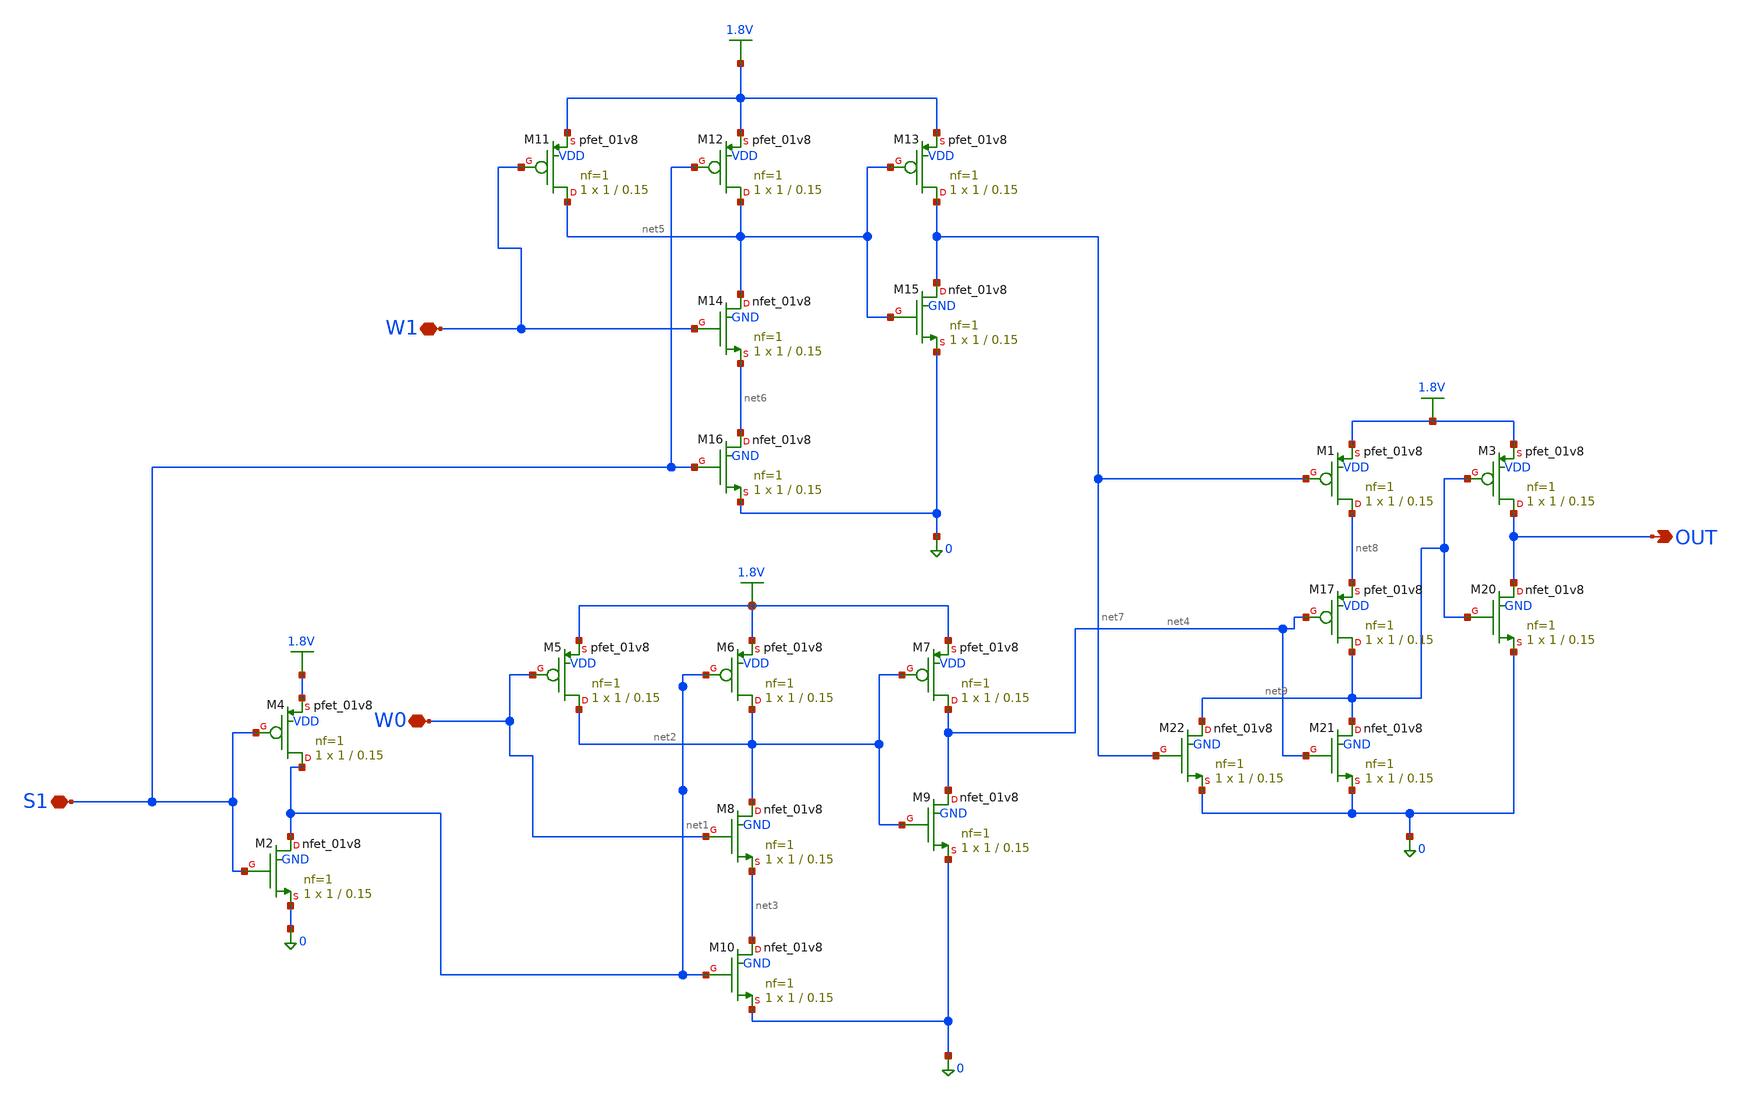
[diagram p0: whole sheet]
** sch_path: XUM21.sch
**.subckt XUM21 OUT W1 W0 S1
*.opin OUT
*.iopin W1
*.iopin W0
*.iopin S1
XM2 net1 S1 0 GND sky130_fd_pr__nfet_01v8 L=0.15 W=1 nf=1 ad='int((1 + 1)/2) * 1 / 1 * 0.29' as='int((1 + 2)/2) * 1 / 1 * 0.29'
+ pd='2*int((1 + 1)/2) * (1 / 1 + 0.29)' ps='2*int((1 + 2)/2) * (1 / 1 + 0.29)' nrd='0.29 / 1 ' nrs='0.29 / 1 '
+ sa=0 sb=0 sd=0 mult=1 m=1
XM8 net2 W0 net3 GND sky130_fd_pr__nfet_01v8 L=0.15 W=1 nf=1 ad='int((1 + 1)/2) * 1 / 1 * 0.29' as='int((1 + 2)/2) * 1 / 1 * 0.29'
+ pd='2*int((1 + 1)/2) * (1 / 1 + 0.29)' ps='2*int((1 + 2)/2) * (1 / 1 + 0.29)' nrd='0.29 / 1 ' nrs='0.29 / 1 '
+ sa=0 sb=0 sd=0 mult=1 m=1
XM9 net4 net2 0 GND sky130_fd_pr__nfet_01v8 L=0.15 W=1 nf=1 ad='int((1 + 1)/2) * 1 / 1 * 0.29' as='int((1 + 2)/2) * 1 / 1 * 0.29'
+ pd='2*int((1 + 1)/2) * (1 / 1 + 0.29)' ps='2*int((1 + 2)/2) * (1 / 1 + 0.29)' nrd='0.29 / 1 ' nrs='0.29 / 1 '
+ sa=0 sb=0 sd=0 mult=1 m=1
XM10 net3 net1 0 GND sky130_fd_pr__nfet_01v8 L=0.15 W=1 nf=1 ad='int((1 + 1)/2) * 1 / 1 * 0.29' as='int((1 + 2)/2) * 1 / 1 * 0.29'
+ pd='2*int((1 + 1)/2) * (1 / 1 + 0.29)' ps='2*int((1 + 2)/2) * (1 / 1 + 0.29)' nrd='0.29 / 1 ' nrs='0.29 / 1 '
+ sa=0 sb=0 sd=0 mult=1 m=1
XM14 net5 W1 net6 GND sky130_fd_pr__nfet_01v8 L=0.15 W=1 nf=1 ad='int((1 + 1)/2) * 1 / 1 * 0.29' as='int((1 + 2)/2) * 1 / 1 * 0.29'
+ pd='2*int((1 + 1)/2) * (1 / 1 + 0.29)' ps='2*int((1 + 2)/2) * (1 / 1 + 0.29)' nrd='0.29 / 1 ' nrs='0.29 / 1 '
+ sa=0 sb=0 sd=0 mult=1 m=1
XM15 net7 net5 0 GND sky130_fd_pr__nfet_01v8 L=0.15 W=1 nf=1 ad='int((1 + 1)/2) * 1 / 1 * 0.29' as='int((1 + 2)/2) * 1 / 1 * 0.29'
+ pd='2*int((1 + 1)/2) * (1 / 1 + 0.29)' ps='2*int((1 + 2)/2) * (1 / 1 + 0.29)' nrd='0.29 / 1 ' nrs='0.29 / 1 '
+ sa=0 sb=0 sd=0 mult=1 m=1
XM16 net6 S1 0 GND sky130_fd_pr__nfet_01v8 L=0.15 W=1 nf=1 ad='int((1 + 1)/2) * 1 / 1 * 0.29' as='int((1 + 2)/2) * 1 / 1 * 0.29'
+ pd='2*int((1 + 1)/2) * (1 / 1 + 0.29)' ps='2*int((1 + 2)/2) * (1 / 1 + 0.29)' nrd='0.29 / 1 ' nrs='0.29 / 1 '
+ sa=0 sb=0 sd=0 mult=1 m=1
XM20 OUT net9 0 GND sky130_fd_pr__nfet_01v8 L=0.15 W=1 nf=1 ad='int((1 + 1)/2) * 1 / 1 * 0.29' as='int((1 + 2)/2) * 1 / 1 * 0.29'
+ pd='2*int((1 + 1)/2) * (1 / 1 + 0.29)' ps='2*int((1 + 2)/2) * (1 / 1 + 0.29)' nrd='0.29 / 1 ' nrs='0.29 / 1 '
+ sa=0 sb=0 sd=0 mult=1 m=1
XM21 net9 net4 0 GND sky130_fd_pr__nfet_01v8 L=0.15 W=1 nf=1 ad='int((1 + 1)/2) * 1 / 1 * 0.29' as='int((1 + 2)/2) * 1 / 1 * 0.29'
+ pd='2*int((1 + 1)/2) * (1 / 1 + 0.29)' ps='2*int((1 + 2)/2) * (1 / 1 + 0.29)' nrd='0.29 / 1 ' nrs='0.29 / 1 '
+ sa=0 sb=0 sd=0 mult=1 m=1
XM22 net9 net7 0 GND sky130_fd_pr__nfet_01v8 L=0.15 W=1 nf=1 ad='int((1 + 1)/2) * 1 / 1 * 0.29' as='int((1 + 2)/2) * 1 / 1 * 0.29'
+ pd='2*int((1 + 1)/2) * (1 / 1 + 0.29)' ps='2*int((1 + 2)/2) * (1 / 1 + 0.29)' nrd='0.29 / 1 ' nrs='0.29 / 1 '
+ sa=0 sb=0 sd=0 mult=1 m=1
XM1 net8 net7 1.8V VDD sky130_fd_pr__pfet_01v8 L=0.15 W=1 nf=1 ad='int((1 + 1)/2) * 1 / 1 * 0.29' as='int((1 + 2)/2) * 1 / 1 * 0.29'
+ pd='2*int((1 + 1)/2) * (1 / 1 + 0.29)' ps='2*int((1 + 2)/2) * (1 / 1 + 0.29)' nrd='0.29 / 1 ' nrs='0.29 / 1 '
+ sa=0 sb=0 sd=0 mult=1 m=1
XM3 OUT net9 1.8V VDD sky130_fd_pr__pfet_01v8 L=0.15 W=1 nf=1 ad='int((1 + 1)/2) * 1 / 1 * 0.29' as='int((1 + 2)/2) * 1 / 1 * 0.29'
+ pd='2*int((1 + 1)/2) * (1 / 1 + 0.29)' ps='2*int((1 + 2)/2) * (1 / 1 + 0.29)' nrd='0.29 / 1 ' nrs='0.29 / 1 '
+ sa=0 sb=0 sd=0 mult=1 m=1
XM11 net5 W1 1.8V VDD sky130_fd_pr__pfet_01v8 L=0.15 W=1 nf=1 ad='int((1 + 1)/2) * 1 / 1 * 0.29' as='int((1 + 2)/2) * 1 / 1 * 0.29'
+ pd='2*int((1 + 1)/2) * (1 / 1 + 0.29)' ps='2*int((1 + 2)/2) * (1 / 1 + 0.29)' nrd='0.29 / 1 ' nrs='0.29 / 1 '
+ sa=0 sb=0 sd=0 mult=1 m=1
XM12 net5 S1 1.8V VDD sky130_fd_pr__pfet_01v8 L=0.15 W=1 nf=1 ad='int((1 + 1)/2) * 1 / 1 * 0.29' as='int((1 + 2)/2) * 1 / 1 * 0.29'
+ pd='2*int((1 + 1)/2) * (1 / 1 + 0.29)' ps='2*int((1 + 2)/2) * (1 / 1 + 0.29)' nrd='0.29 / 1 ' nrs='0.29 / 1 '
+ sa=0 sb=0 sd=0 mult=1 m=1
XM13 net7 net5 1.8V VDD sky130_fd_pr__pfet_01v8 L=0.15 W=1 nf=1 ad='int((1 + 1)/2) * 1 / 1 * 0.29' as='int((1 + 2)/2) * 1 / 1 * 0.29'
+ pd='2*int((1 + 1)/2) * (1 / 1 + 0.29)' ps='2*int((1 + 2)/2) * (1 / 1 + 0.29)' nrd='0.29 / 1 ' nrs='0.29 / 1 '
+ sa=0 sb=0 sd=0 mult=1 m=1
XM5 net2 W0 1.8V VDD sky130_fd_pr__pfet_01v8 L=0.15 W=1 nf=1 ad='int((1 + 1)/2) * 1 / 1 * 0.29' as='int((1 + 2)/2) * 1 / 1 * 0.29'
+ pd='2*int((1 + 1)/2) * (1 / 1 + 0.29)' ps='2*int((1 + 2)/2) * (1 / 1 + 0.29)' nrd='0.29 / 1 ' nrs='0.29 / 1 '
+ sa=0 sb=0 sd=0 mult=1 m=1
XM6 net2 net1 1.8V VDD sky130_fd_pr__pfet_01v8 L=0.15 W=1 nf=1 ad='int((1 + 1)/2) * 1 / 1 * 0.29' as='int((1 + 2)/2) * 1 / 1 * 0.29'
+ pd='2*int((1 + 1)/2) * (1 / 1 + 0.29)' ps='2*int((1 + 2)/2) * (1 / 1 + 0.29)' nrd='0.29 / 1 ' nrs='0.29 / 1 '
+ sa=0 sb=0 sd=0 mult=1 m=1
XM7 net4 net2 1.8V VDD sky130_fd_pr__pfet_01v8 L=0.15 W=1 nf=1 ad='int((1 + 1)/2) * 1 / 1 * 0.29' as='int((1 + 2)/2) * 1 / 1 * 0.29'
+ pd='2*int((1 + 1)/2) * (1 / 1 + 0.29)' ps='2*int((1 + 2)/2) * (1 / 1 + 0.29)' nrd='0.29 / 1 ' nrs='0.29 / 1 '
+ sa=0 sb=0 sd=0 mult=1 m=1
XM4 net1 S1 1.8V VDD sky130_fd_pr__pfet_01v8 L=0.15 W=1 nf=1 ad='int((1 + 1)/2) * 1 / 1 * 0.29' as='int((1 + 2)/2) * 1 / 1 * 0.29'
+ pd='2*int((1 + 1)/2) * (1 / 1 + 0.29)' ps='2*int((1 + 2)/2) * (1 / 1 + 0.29)' nrd='0.29 / 1 ' nrs='0.29 / 1 '
+ sa=0 sb=0 sd=0 mult=1 m=1
XM17 net9 net4 net8 VDD sky130_fd_pr__pfet_01v8 L=0.15 W=1 nf=1 ad='int((1 + 1)/2) * 1 / 1 * 0.29' as='int((1 + 2)/2) * 1 / 1 * 0.29'
+ pd='2*int((1 + 1)/2) * (1 / 1 + 0.29)' ps='2*int((1 + 2)/2) * (1 / 1 + 0.29)' nrd='0.29 / 1 ' nrs='0.29 / 1 '
+ sa=0 sb=0 sd=0 mult=1 m=1
**.ends
.GLOBAL 1.8V
.end
